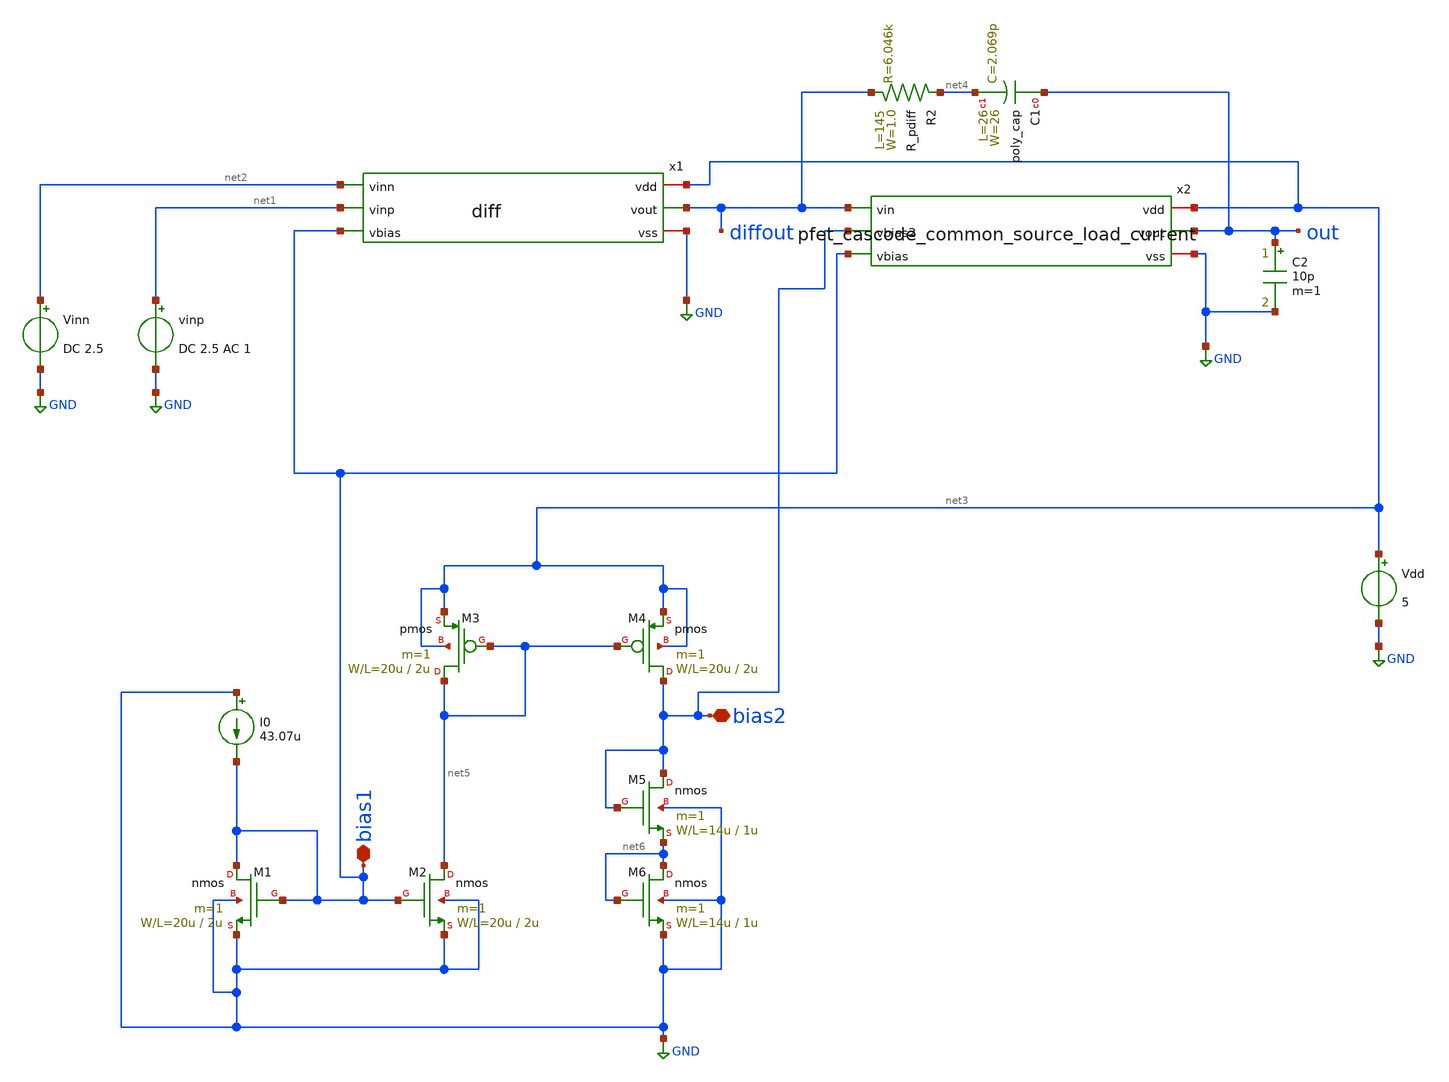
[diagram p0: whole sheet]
** sch_path: member_project/GroupWork/Team_masahiro/diff+cascode_source_common+bias.sch
**.subckt diff+cascode_source_common+bias bias1 bias2
*.iopin bias1
*.iopin bias2
x1 net3 diffout net2 net1 bias1 GND diff
Vinn net2 GND DC 2.5
vinp net1 GND DC 2.5 AC 1
Vdd net3 GND 5
x2 net3 diffout bias2 out bias1 GND pfet_cascode_common_source_load_current
C2 out GND 10p m=1
C1 out net4 poly_cap W=26 L=26
R2 diffout net4 R_pdiff W=1.0 L=145
M1 bias1 bias1 GND GND nmos L=2u W=20u m=1
M2 net5 bias1 GND GND nmos L=2u W=20u m=1
M3 net5 net5 net3 net3 pmos L=2u W=20u m=1
M4 bias2 net5 net3 net3 pmos L=2u W=20u m=1
M5 bias2 bias2 net6 GND nmos L=1u W=14u m=1
M6 net6 net6 GND GND nmos L=1u W=14u m=1
I0 GND bias1 43.07u
**** begin user architecture code
 .include $::LIB/mos.lib
.include $::LIB/passive.lib
.include $::LIB/diode.lib


.option savecurrent
.control
set units=degree
op
#show m
print bias1
print bias2
save all
ac dec 20 1e3 1e10
plot vdb(out) vdb(diffout)
plot vp(out) vp(diffout)
print @m.x1.m2[vgs]
print @m.x1.m2[vds]
print @m.x1.m2[vth]
print @m.x1.m2[vgs] - @m.x1.m2[vth]
print @m.x1.m2[gm]
print @m.x1.m2[gds]
print @m.x1.m5[vgs]
print @m.x1.m5[vds]
print @m.x1.m5[vth]
print @m.x1.m5[vgs] - @m.x1.m5[vth]
print @m.x1.m5[gm]
print @m.x1.m5[gds]
print @m.x1.m3[vgs]
print @m.x1.m3[vds]
print @m.x1.m3[vth]
print @m.x1.m3[vgs] - @m.x1.m3[vth]
print @m.x1.m3[gm]
print @m.x1.m3[gds]
print @m.x1.m3[vds] + @m.x1.m2[vds]

.endc




.measure ac gain find vdb(out) at=1e3
.measure ac ugf when vdb(out)=0
.measure ac phase find vp(out) at = 30.e6


**** end user architecture code
**.ends

* expanding   symbol:  diff.sym # of pins=6
** sym_path: member_project/GroupWork/Team_masahiro/diff.sym
** sch_path: member_project/GroupWork/Team_masahiro/diff.sch
.subckt diff vdd vout vinn vinp vbias vss
*.iopin vss
*.iopin vdd
*.ipin vinn
*.ipin vinp
*.opin vout
*.ipin vbias
M1 net1 vinn net2 vss nmos L=2u W=100u m=1
M2 vout vinp net2 vss nmos L=2u W=100u m=1
M3 net2 vbias vss vss nmos L=2u W=20u m=1
M4 net1 net1 vdd vdd pmos L=2u W=35u m=1
M5 vout net1 vdd vdd pmos L=2u W=35u m=1
.ends


* expanding   symbol:  pfet_cascode_common_source_load_current.sym # of pins=6
** sym_path: member_project/GroupWork/Team_masahiro/pfet_cascode_common_source_load_current.sym
** sch_path: member_project/GroupWork/Team_masahiro/pfet_cascode_common_source_load_current.sch
.subckt pfet_cascode_common_source_load_current vdd vin vbias2 vout vbias vss
*.iopin vss
*.iopin vdd
*.ipin vin
*.opin vout
*.ipin vbias
*.ipin vbias2
M1 vout vbias vss vss nmos L=1u W=80u m=1
M2 net1 vin vdd vdd pmos L=1u W=160u m=1
M3 vout vbias2 net1 net1 pmos L=1u W=160u m=1
.ends

.GLOBAL GND
.end
